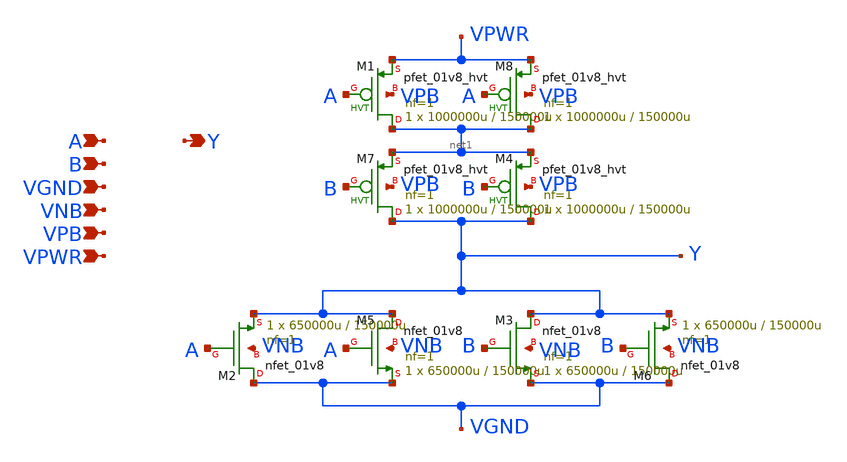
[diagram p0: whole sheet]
** sch_path: schematics/nor2/sky130_fd_sc_hd__nor2_2.sch
**.subckt sky130_fd_sc_hd__nor2_2 A B VGND VNB VPB VPWR Y
*.ipin A
*.ipin B
*.ipin VGND
*.ipin VNB
*.ipin VPB
*.ipin VPWR
*.opin Y
XM2 VGND A Y VNB sky130_fd_pr__nfet_01v8 L=150000u W=650000u nf=1 ad='int((1 + 1)/2) * 650000u / 1 * 0.29'
+ as='int((1 + 2)/2) * 650000u / 1 * 0.29' pd='2*int((1 + 1)/2) * (650000u / 1 + 0.29)' ps='2*int((1 + 2)/2) * (650000u / 1 + 0.29)'
+ nrd='0.29 / 650000u ' nrs='0.29 / 650000u ' sa=0 sb=0 sd=0 mult=1 m=1
XM3 Y B VGND VNB sky130_fd_pr__nfet_01v8 L=150000u W=650000u nf=1 ad='int((1 + 1)/2) * 650000u / 1 * 0.29'
+ as='int((1 + 2)/2) * 650000u / 1 * 0.29' pd='2*int((1 + 1)/2) * (650000u / 1 + 0.29)' ps='2*int((1 + 2)/2) * (650000u / 1 + 0.29)'
+ nrd='0.29 / 650000u ' nrs='0.29 / 650000u ' sa=0 sb=0 sd=0 mult=1 m=1
XM5 Y A VGND VNB sky130_fd_pr__nfet_01v8 L=150000u W=650000u nf=1 ad='int((1 + 1)/2) * 650000u / 1 * 0.29'
+ as='int((1 + 2)/2) * 650000u / 1 * 0.29' pd='2*int((1 + 1)/2) * (650000u / 1 + 0.29)' ps='2*int((1 + 2)/2) * (650000u / 1 + 0.29)'
+ nrd='0.29 / 650000u ' nrs='0.29 / 650000u ' sa=0 sb=0 sd=0 mult=1 m=1
XM6 VGND B Y VNB sky130_fd_pr__nfet_01v8 L=150000u W=650000u nf=1 ad='int((1 + 1)/2) * 650000u / 1 * 0.29'
+ as='int((1 + 2)/2) * 650000u / 1 * 0.29' pd='2*int((1 + 1)/2) * (650000u / 1 + 0.29)' ps='2*int((1 + 2)/2) * (650000u / 1 + 0.29)'
+ nrd='0.29 / 650000u ' nrs='0.29 / 650000u ' sa=0 sb=0 sd=0 mult=1 m=1
XM1 net1 A VPWR VPB sky130_fd_pr__pfet_01v8_hvt L=150000u W=1000000u nf=1 ad='int((1 + 1)/2) * 1000000u / 1 * 0.29'
+ as='int((1 + 2)/2) * 1000000u / 1 * 0.29' pd='2*int((1 + 1)/2) * (1000000u / 1 + 0.29)' ps='2*int((1 + 2)/2) * (1000000u / 1 + 0.29)'
+ nrd='0.29 / 1000000u ' nrs='0.29 / 1000000u ' sa=0 sb=0 sd=0 mult=1 m=1
XM4 Y B net1 VPB sky130_fd_pr__pfet_01v8_hvt L=150000u W=1000000u nf=1 ad='int((1 + 1)/2) * 1000000u / 1 * 0.29'
+ as='int((1 + 2)/2) * 1000000u / 1 * 0.29' pd='2*int((1 + 1)/2) * (1000000u / 1 + 0.29)' ps='2*int((1 + 2)/2) * (1000000u / 1 + 0.29)'
+ nrd='0.29 / 1000000u ' nrs='0.29 / 1000000u ' sa=0 sb=0 sd=0 mult=1 m=1
XM7 Y B net1 VPB sky130_fd_pr__pfet_01v8_hvt L=150000u W=1000000u nf=1 ad='int((1 + 1)/2) * 1000000u / 1 * 0.29'
+ as='int((1 + 2)/2) * 1000000u / 1 * 0.29' pd='2*int((1 + 1)/2) * (1000000u / 1 + 0.29)' ps='2*int((1 + 2)/2) * (1000000u / 1 + 0.29)'
+ nrd='0.29 / 1000000u ' nrs='0.29 / 1000000u ' sa=0 sb=0 sd=0 mult=1 m=1
XM8 net1 A VPWR VPB sky130_fd_pr__pfet_01v8_hvt L=150000u W=1000000u nf=1 ad='int((1 + 1)/2) * 1000000u / 1 * 0.29'
+ as='int((1 + 2)/2) * 1000000u / 1 * 0.29' pd='2*int((1 + 1)/2) * (1000000u / 1 + 0.29)' ps='2*int((1 + 2)/2) * (1000000u / 1 + 0.29)'
+ nrd='0.29 / 1000000u ' nrs='0.29 / 1000000u ' sa=0 sb=0 sd=0 mult=1 m=1
**.ends
.end
